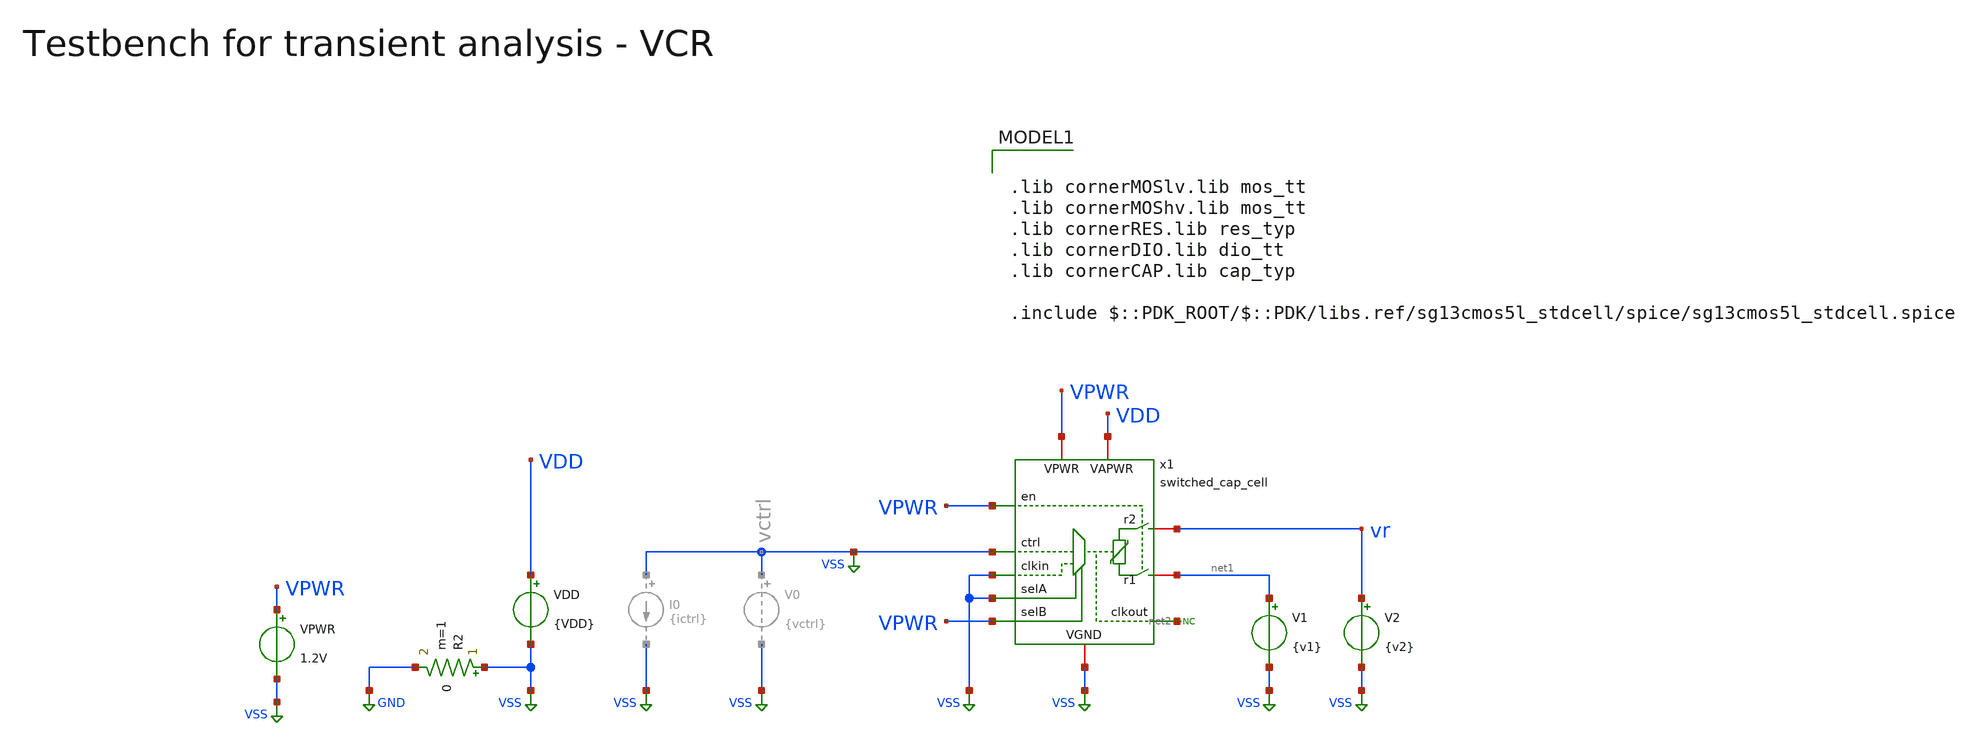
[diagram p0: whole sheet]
** sch_path: macros/heichips26_vcr/macros/switched_capacitor/testbenches/xschem/tb_switched_cap_tran.sch
**.subckt tb_switched_cap_tran
VDD VDD VSS {VDD}
R2 VSS GND 0 m=1
x1 VSS VDD VSS vr net1 VSS VSS VPWR VPWR VPWR net2 switched_cap_cell
V1 net1 VSS {v1}
V2 vr VSS {v2}
VPWR VPWR VSS 1.2V
* noconn #net2
**** begin user architecture code

.lib cornerMOSlv.lib mos_tt
.lib cornerMOShv.lib mos_tt
.lib cornerRES.lib res_typ
.lib cornerDIO.lib dio_tt
.lib cornerCAP.lib cap_typ

.include $::PDK_ROOT/$::PDK/libs.ref/sg13cmos5l_stdcell/spice/sg13cmos5l_stdcell.spice



.param temp=27
.param vctrl  = 0.1
.param f      = {2e6/vctrl}
*.param f = 75Meg

* Derived timing parameters
.param period = {1/f}
.param ton    = {period/2}
.csparam tstop  = {5*period}
.csparam tstep  = {period/100}
.param ictrl  = {f*3.3e-12}
.param tr     = {period/1000}
.param tf     = {period/1000}

.param VDD = 3.3
.csparam VDD=VDD
.param vdm = 3.3
.param vcm = {VDD/2}
.param v1  = {vcm - vdm/2}
.param v2  = {vcm + vdm/2}

.options savecurrents klu method=gear reltol=1e-6 abstol=1e-12 gmin=1e-15
.probe alli
.control

save all
set appendwrite

tran {$&tstep} {$&tstop}
remzerovec

save all
set appendwrite

write @schname\.raw
set appendwrite

*let r_var = vr/i(r1)
meas tran period_sim TRIG i(V1) VAL=1m RISE=1 TARG i(V1) VAL=1m RISE=2
meas tran n_periods TRIG i(V1) VAL=1m RISE=1 TARG i(V1) VAL=1m RISE=LAST
meas tran i_avg AVG i(V1) FROM=0 TO=n_periods
meas tran v_avg AVG vr FROM=0 TO=n_periods
*meas tran r_avg AVG r_var

let npts = length(time) - 1
let i_mavg = integ(i(V1))[1, npts] / time[1, npts]
let v_mavg = integ(vr)[1, npts] / time[1, npts]
let r_mavg = v_mavg/i_mavg
let r_avg = v_avg/i_avg
let f_sim = 1/period_sim
let plot_y_lim = 1.2*r_avg

print period_sim f_sim r_avg

* Plotting
plot vr v_avg v_mavg
plot i(V1) i_avg i_mavg
plot r_avg r_mavg ylimit 0 $&plot_y_lim
plot x1.clk

* Write Data
unset appendwrite
set wr_vecnames
set wr_singlescale
wrdata ../plot_simulations/data/@schname\.txt v(vr) v(VDD) i(V1)

*quit
.endc


**** end user architecture code
**.ends

* expanding   symbol:  switched_cap_cell.sym # of pins=11
** sym_path: macros/heichips26_vcr/macros/switched_capacitor/schematic/xschem/switched_cap_cell.sym
** sch_path: macros/heichips26_vcr/macros/switched_capacitor/schematic/xschem/switched_cap_cell.sch
.subckt switched_cap_cell ctrl VAPWR VGND r2 r1 clkin selA selB en VPWR clkout
*.iopin r1
*.iopin r2
*.iopin VAPWR
*.iopin VGND
*.ipin ctrl
*.ipin clkin
*.ipin selA
*.ipin selB
*.ipin en
*.opin clkout
*.iopin VPWR
x2 out1 r1 c_sw nout1 VAPWR VGND transmission_gate
x6 out2 r2 c_sw nout2 VAPWR VGND transmission_gate
x1 VAPWR net3 net9 VGND net15 net16 osc
x4 net5 VAPWR clk VGND net3 net13 net1 net2 net6 net7 net8 hv_mux4
x5 VAPWR net2 VGND net17 net1 net18 vco
x3 out1 nout1 VAPWR clk VGND out2 nout2 net4 net14 pulse_shaper_en
x7 net11 net10 net5 net6 VAPWR VGND net7 net8 hv_binary_decoder4
* noconn #net18
* noconn #net19
* noconn #net15
* noconn #net16
* noconn #net17
x8 net12 ctrl net9 net7 VAPWR VGND transmission_gate
x9 VAPWR net7 net12 VGND hv_inverter_40u
x10 VAPWR clkin net13 VGND lvl_shift_up
x11 VAPWR selA net10 VGND lvl_shift_up
x12 VAPWR selB net11 VGND lvl_shift_up
x13 VAPWR en net4 VGND lvl_shift_up
x14 VPWR clk clkout VGND hv_inverter_40u
x15 VAPWR net4 net14 VGND hv_inverter_40u
x16 net4 ctrl net1 net14 VAPWR VGND transmission_gate
.ends


* expanding   symbol:  transmission_gate.sym # of pins=6
** sym_path: macros/heichips26_vcr/macros/switched_capacitor/schematic/xschem/transmission_gate.sym
** sch_path: macros/heichips26_vcr/macros/switched_capacitor/schematic/xschem/transmission_gate.sch
.subckt transmission_gate vctrl vin vout nvctrl VDD VSS
*.iopin vin
*.iopin vout
*.ipin vctrl
*.ipin nvctrl
*.iopin VDD
*.iopin VSS
XM3 vout vctrl vin VSS sg13_hv_nmos w={tg_ngate_w*tg_ng} l={tg_ch_len} ng={tg_ng} m=1 mm_ok=1
XM4 vout nvctrl vin VDD sg13_hv_pmos w={tg_pgate_w*tg_ng} l={tg_ch_len} ng={tg_ng} m=1 mm_ok=1
**** begin user architecture code


.param tg_ch_len=0.45u
.param tg_ngate_w=2u
.param tg_pgate_w=5u
.param tg_ng=20


**** end user architecture code
.ends


* expanding   symbol:  osc.sym # of pins=6
** sym_path: macros/heichips26_vcr/macros/switched_capacitor/schematic/xschem/osc.sym
** sch_path: macros/heichips26_vcr/macros/switched_capacitor/schematic/xschem/osc.sch
.subckt osc VDD out1 ictrl VSS start out2
*.iopin VSS
*.iopin VDD
*.iopin out2
*.iopin out1
*.iopin start
*.iopin ictrl
XM3 out1 ictrl VDD VDD sg13_hv_pmos w=10.0u l=2.0u ng=1 m=1 mm_ok=1
XM2 net1 ictrl VDD VDD sg13_hv_pmos w=1u l=2.0u ng=1 m=1 mm_ok=1
XM4 start ictrl VDD VDD sg13_hv_pmos w=1.0u l=2.0u ng=1 m=1 mm_ok=1
XM5 out2 ictrl VDD VDD sg13_hv_pmos w=10.0u l=2.0u ng=1 m=1 mm_ok=1
XM6 ictrl ictrl VDD VDD sg13_hv_pmos w=10.0u l=2.0u ng=1 m=1 mm_ok=1
XC1 net1 out1 cap_cmomi w=10e-6 l=10e-6 mmin=1 mmax=4 feed=double subblock=0 m=1 mm_ok=1
XC2 out2 start cap_cmomi w=10e-6 l=10e-6 mmin=1 mmax=4 feed=double subblock=0 m=1 mm_ok=1
XM8 out1 start VSS VSS sg13_hv_nmos w=3u l=0.45u ng=1 m=1 mm_ok=1
XM1 start start VSS VSS sg13_hv_nmos w=1u l=2u ng=1 m=1 mm_ok=1
XM12 out2 net1 VSS VSS sg13_hv_nmos w=3u l=0.45u ng=1 m=1 mm_ok=1
XM11 net1 net1 VSS VSS sg13_hv_nmos w=1u l=2u ng=1 m=1 mm_ok=1
**** begin user architecture code


.ic v(out1)=0 v(out2)=3.3


**** end user architecture code
.ends


* expanding   symbol:  hv_mux4.sym # of pins=11
** sym_path: macros/heichips26_vcr/macros/switched_capacitor/schematic/xschem/hv_mux4.sym
** sch_path: macros/heichips26_vcr/macros/switched_capacitor/schematic/xschem/hv_mux4.sch
.subckt hv_mux4 nsel1 VDD out VSS in3 in1 in4 in2 nsel2 nsel3 nsel4
*.ipin in1
*.iopin VDD
*.iopin VSS
*.opin out
*.ipin in2
*.ipin in3
*.ipin in4
*.ipin nsel1
*.ipin nsel3
*.ipin nsel2
*.ipin nsel4
x1 VDD net2 out net1 VSS net3 net4 hv_nor4
x2 VDD nsel1 net2 in1 VSS hv_nor
x4 VDD nsel2 net1 in2 VSS hv_nor
x5 VDD nsel3 net3 in3 VSS hv_nor
x6 VDD nsel4 net4 in4 VSS hv_nor
.ends


* expanding   symbol:  vco.sym # of pins=6
** sym_path: macros/heichips26_vcr/macros/switched_capacitor/schematic/xschem/vco.sym
** sch_path: macros/heichips26_vcr/macros/switched_capacitor/schematic/xschem/vco.sch
.subckt vco VDD out VSS nout vctrl vc
*.iopin VSS
*.iopin VDD
*.iopin nout
*.iopin out
*.iopin vctrl
*.iopin vc
**** begin user architecture code


.ic v(vc)=1.65


**** end user architecture code
XC1 vc VSS cap_cmomi w=30e-6 l=30e-6 mmin=1 mmax=4 feed=double subblock=0 m=1 mm_ok=1
XM4 vc out 5uA- VSS sg13_hv_nmos w=0.3u l=0.45u ng=1 m=1 mm_ok=1
x1 VDD s out nout r VSS hv_rs-ff
**** begin user architecture code


.param cm_n_w = 6u
.param cm_n_l = 5u
.param cm_p_w = 10u
.param cm_p_l = 2u

.param inv_ng = 1
.param inv_n_w = 2u
.param inv_n_l = 0.45u
.param inv_p_w = 6.5u
.param inv_p_l = 0.4u


**** end user architecture code
XM6 vc out 5uA+ VDD sg13_hv_pmos w=0.3u l=0.4u ng=1 m=1 mm_ok=1
x5 net2 vc vthl VDD 40uA- VSS comp_pmos
x7 net1 vthh vc VDD 40uA+ VSS comp_nmos
x2 10uA- vthl VDD vctrl VSS vthh voltage_mirror_pmos
x3 VDD net1 s VSS hv_inverter_6u5
x6 VDD net2 r VSS hv_inverter_6u5
x8 40uA+ 5uA+ VDD VSS 5uA- 10uA- 40uA- bias_current_generator
.ends


* expanding   symbol:  pulse_shaper_en.sym # of pins=9
** sym_path: macros/heichips26_vcr/macros/switched_capacitor/schematic/xschem/pulse_shaper_en.sym
** sch_path: macros/heichips26_vcr/macros/switched_capacitor/schematic/xschem/pulse_shaper_en.sch
.subckt pulse_shaper_en out1 nout1 VDD in VSS out2 nout2 en dis
*.opin out1
*.opin nout1
*.opin out2
*.opin nout2
*.ipin in
*.iopin VSS
*.iopin VDD
*.ipin en
*.ipin dis
x7 VDD net1 net3 VSS low_th_inverter
x8 VDD net1 net2 VSS high_th_inverter
x10 VDD out1 nout1 VSS hv_inverter_40u
x11 VDD nout2 out2 VSS hv_inverter_40u
**** begin user architecture code


.include ../../../netlist/pex/hv_inverter_0u3_magic_pex_3.spice
.param w   = 0.3u
.param ng  = 1
.param n_ng = ng
.param n_w = {w*n_ng}
.param n_l = 0.45u
.param p_ng = ng
.param p_w = {1*w*p_ng}
.param p_l = 0.4u


**** end user architecture code
x1 VDD in net1 VSS hv_inverter_0u3
x5 VDD net2 out1 dis VSS hv_nor
x4 VDD net3 nout2 en VSS hv_nand
.ends


* expanding   symbol:  hv_binary_decoder4.sym # of pins=8
** sym_path: macros/heichips26_vcr/macros/switched_capacitor/schematic/xschem/hv_binary_decoder4.sym
** sch_path: macros/heichips26_vcr/macros/switched_capacitor/schematic/xschem/hv_binary_decoder4.sch
.subckt hv_binary_decoder4 msb lsb nout1 nout2 VDD VSS nout3 nout4
*.iopin VDD
*.iopin VSS
*.ipin msb
*.ipin lsb
*.opin nout1
*.opin nout2
*.opin nout3
*.opin nout4
x3 VDD msb net1 VSS hv_inverter_40u
x7 VDD msb nout4 lsb VSS hv_nand
x9 VDD net1 nout2 lsb VSS hv_nand
x10 VDD lsb net2 VSS hv_inverter_40u
x11 VDD msb nout3 net2 VSS hv_nand
x8 VDD net1 nout1 net2 VSS hv_nand
.ends


* expanding   symbol:  hv_inverter_40u.sym # of pins=4
** sym_path: macros/heichips26_vcr/macros/switched_capacitor/schematic/xschem/hv_inverter_40u.sym
** sch_path: macros/heichips26_vcr/macros/switched_capacitor/schematic/xschem/hv_inverter_40u.sch
.subckt hv_inverter_40u VDD in out VSS
*.ipin in
*.iopin VDD
*.iopin VSS
*.opin out
XM2 out in VSS VSS sg13_hv_nmos w={n_w} l={n_l} ng={ng} m=1 mm_ok=1
XM3 out in VDD VDD sg13_hv_pmos w={p_w} l={p_l} ng={ng} m=1 mm_ok=1
**** begin user architecture code


.param w   = 10u
.param ng  = 4
.param n_ng = ng
.param n_w = {3u*n_ng}
.param n_l = 0.45u
.param p_ng = ng
.param p_w = {10u*p_ng}
.param p_l = 0.4u


**** end user architecture code
.ends


* expanding   symbol:  lvl_shift_up.sym # of pins=4
** sym_path: macros/heichips26_vcr/macros/switched_capacitor/schematic/xschem/lvl_shift_up.sym
** sch_path: macros/heichips26_vcr/macros/switched_capacitor/schematic/xschem/lvl_shift_up.sch
.subckt lvl_shift_up VDD in out VSS
*.ipin in
*.iopin VDD
*.iopin VSS
*.opin out
XM1 net1 in VSS VSS sg13_hv_nmos w={n_ng*n_w} l={n_l} ng={n_ng} m=1 mm_ok=1
XM2 net1 in VDD VDD sg13_hv_pmos w={p_ng*p_w} l={p_l} ng={n_ng} m=1 mm_ok=1
**** begin user architecture code


.param n_ng = 2
.param n_w = 10u
.param n_l = 0.45u
.param p_ng = 2
.param p_w = 1u
.param p_l = 0.45u


**** end user architecture code
x4 VDD net1 out VSS hv_inverter_6u5
.ends


* expanding   symbol:  hv_nor4.sym # of pins=7
** sym_path: macros/heichips26_vcr/macros/switched_capacitor/schematic/xschem/hv_nor4.sym
** sch_path: macros/heichips26_vcr/macros/switched_capacitor/schematic/xschem/hv_nor4.sch
.subckt hv_nor4 VDD in1 out in2 VSS in3 in4
*.ipin in1
*.iopin VDD
*.iopin VSS
*.opin out
*.ipin in2
*.ipin in3
*.ipin in4
**** begin user architecture code


.param w   = 10u
.param ng  = 4
.param n_ng = ng
.param n_w = {3u*n_ng}
.param n_l = 0.45u
.param p_ng = ng
.param p_w = {10u*p_ng}
.param p_l = 0.4u


**** end user architecture code
XM2 out in3 VSS VSS sg13_hv_nmos w={n_w} l={n_l} ng={ng} m=1 mm_ok=1
XM3 net3 in4 VDD VDD sg13_hv_pmos w={p_w} l={p_l} ng={ng} m=1 mm_ok=1
XM1 out in4 VSS VSS sg13_hv_nmos w={n_w} l={n_l} ng={ng} m=1 mm_ok=1
XM4 out in1 net1 VDD sg13_hv_pmos w={p_w} l={p_l} ng={ng} m=1 mm_ok=1
XM5 out in2 VSS VSS sg13_hv_nmos w={n_w} l={n_l} ng={ng} m=1 mm_ok=1
XM6 out in1 VSS VSS sg13_hv_nmos w={n_w} l={n_l} ng={ng} m=1 mm_ok=1
XM7 net1 in2 net2 VDD sg13_hv_pmos w={p_w} l={p_l} ng={ng} m=1 mm_ok=1
XM8 net2 in3 net3 VDD sg13_hv_pmos w={p_w} l={p_l} ng={ng} m=1 mm_ok=1
.ends


* expanding   symbol:  hv_nor.sym # of pins=5
** sym_path: macros/heichips26_vcr/macros/switched_capacitor/schematic/xschem/hv_nor.sym
** sch_path: macros/heichips26_vcr/macros/switched_capacitor/schematic/xschem/hv_nor.sch
.subckt hv_nor VDD in1 out in2 VSS
*.ipin in1
*.iopin VDD
*.iopin VSS
*.opin out
*.ipin in2
**** begin user architecture code


.param w   = 10u
.param ng  = 4
.param n_ng = ng
.param n_w = {3u*n_ng}
.param n_l = 0.45u
.param p_ng = ng
.param p_w = {10u*p_ng}
.param p_l = 0.4u


**** end user architecture code
XM2 out in1 VSS VSS sg13_hv_nmos w={n_w} l={n_l} ng={ng} m=1 mm_ok=1
XM3 net1 in2 VDD VDD sg13_hv_pmos w={p_w} l={p_l} ng={ng} m=1 mm_ok=1
XM1 out in2 VSS VSS sg13_hv_nmos w={n_w} l={n_l} ng={ng} m=1 mm_ok=1
XM4 out in1 net1 VDD sg13_hv_pmos w={p_w} l={p_l} ng={ng} m=1 mm_ok=1
.ends


* expanding   symbol:  hv_rs-ff.sym # of pins=6
** sym_path: macros/heichips26_vcr/macros/switched_capacitor/schematic/xschem/hv_rs-ff.sym
** sch_path: macros/heichips26_vcr/macros/switched_capacitor/schematic/xschem/hv_rs-ff.sch
.subckt hv_rs-ff VDD nS Q nQ nR VSS
*.ipin nS
*.iopin VDD
*.iopin VSS
*.opin Q
*.ipin nR
*.opin nQ
x4 VDD nS Q nQ VSS hv_nand
x5 VDD Q nQ nR VSS hv_nand
.ends


* expanding   symbol:  comp_pmos.sym # of pins=6
** sym_path: macros/heichips26_vcr/macros/switched_capacitor/schematic/xschem/comp_pmos.sym
** sch_path: macros/heichips26_vcr/macros/switched_capacitor/schematic/xschem/comp_pmos.sch
.subckt comp_pmos out - + VDD Ibias VSS
*.iopin VDD
*.iopin VSS
*.ipin Ibias
*.opin out
*.ipin +
*.ipin -
**** begin user architecture code


.param n_w = 1.2u
.param n_l = 1.5u
.param p_w = 2u
.param p_l = 0.4u
.param bcm = 1


**** end user architecture code
XM9 net1 Ibias VDD VDD sg13_hv_pmos w=bcm*p_w l=p_l ng=1 m=1 mm_ok=1
XM10 out Ibias VDD VDD sg13_hv_pmos w=bcm*p_w l=p_l ng=1 m=1 mm_ok=1
XM11 Ibias Ibias VDD VDD sg13_hv_pmos w=p_w l=p_l ng=1 m=1 mm_ok=1
XM12 net3 + net1 VDD sg13_hv_pmos w=p_w l=p_l ng=1 m=1 mm_ok=1
XM13 net2 - net1 VDD sg13_hv_pmos w=p_w l=p_l ng=1 m=1 mm_ok=1
XM14 net3 net2 VSS VSS sg13_hv_nmos w=n_w l=n_l ng=1 m=1 mm_ok=1
XM15 net2 net2 VSS VSS sg13_hv_nmos w=n_w l=n_l ng=1 m=1 mm_ok=1
XM16 out net3 VSS VSS sg13_hv_nmos w=n_w l=n_l ng=1 m=1 mm_ok=1
.ends


* expanding   symbol:  comp_nmos.sym # of pins=6
** sym_path: macros/heichips26_vcr/macros/switched_capacitor/schematic/xschem/comp_nmos.sym
** sch_path: macros/heichips26_vcr/macros/switched_capacitor/schematic/xschem/comp_nmos.sch
.subckt comp_nmos out - + VDD Ibias VSS
*.iopin VDD
*.iopin VSS
*.ipin -
*.ipin +
*.ipin Ibias
*.opin out
XM8 net2 + net3 VSS sg13_hv_nmos w=n_w l=n_l ng=1 m=1 mm_ok=1
XM6 net1 net1 VDD VDD sg13_hv_pmos w=p_w l=p_l ng=1 m=1 mm_ok=1
XM1 net2 net1 VDD VDD sg13_hv_pmos w=p_w l=p_l ng=1 m=1 mm_ok=1
XM3 net1 - net3 VSS sg13_hv_nmos w=n_w l=n_l ng=1 m=1 mm_ok=1
**** begin user architecture code


.param n_w = 1.2u
.param n_l = 1.5u
.param p_w = 2u
.param p_l = 0.4u


**** end user architecture code
XM2 out net2 VDD VDD sg13_hv_pmos w=p_w l=p_l ng=1 m=1 mm_ok=1
XM4 net3 Ibias VSS VSS sg13_hv_nmos w=2*n_w l=n_l ng=1 m=1 mm_ok=1
XM5 out Ibias VSS VSS sg13_hv_nmos w=2*n_w l=n_l ng=1 m=1 mm_ok=1
XM7 Ibias Ibias VSS VSS sg13_hv_nmos w=n_w l=n_l ng=1 m=1 mm_ok=1
.ends


* expanding   symbol:  voltage_mirror_pmos.sym # of pins=6
** sym_path: macros/heichips26_vcr/macros/switched_capacitor/schematic/xschem/voltage_mirror_pmos.sym
** sch_path: macros/heichips26_vcr/macros/switched_capacitor/schematic/xschem/voltage_mirror_pmos.sch
.subckt voltage_mirror_pmos Ibias nout VDD in VSS out
*.iopin VDD
*.iopin VSS
*.ipin in
*.opin out
*.opin nout
*.ipin Ibias
**** begin user architecture code


.param n_w = 6u
.param n_l = 5u
.param p_w = 10u
.param p_l = 2u


**** end user architecture code
XR1 in Ibias VSS rhigh w=0.5e-6 l=34e-6 m=1 b=0 mm_ok=1
XM4 net1 Ibias VDD VDD sg13_hv_pmos w=p_w l=p_l ng=1 m=1 mm_ok=1
XM5 out net1 VSS VSS sg13_hv_nmos w=n_w l=n_l ng=1 m=1 mm_ok=1
XR2 VSS nout VSS rhigh w=0.5e-6 l=34e-6 m=1 b=0 mm_ok=1
XR3 out VDD VSS rhigh w=0.5e-6 l=34e-6 m=1 b=0 mm_ok=1
XM2 net1 net1 VSS VSS sg13_hv_nmos w=n_w l=n_l ng=1 m=1 mm_ok=1
XM3 nout Ibias VDD VDD sg13_hv_pmos w=p_w l=p_l ng=1 m=1 mm_ok=1
XM6 Ibias Ibias VDD VDD sg13_hv_pmos w=1.9*p_w l=p_l ng=1 m=1 mm_ok=1
.ends


* expanding   symbol:  hv_inverter_6u5.sym # of pins=4
** sym_path: macros/heichips26_vcr/macros/switched_capacitor/schematic/xschem/hv_inverter_6u5.sym
** sch_path: macros/heichips26_vcr/macros/switched_capacitor/schematic/xschem/hv_inverter_6u5.sch
.subckt hv_inverter_6u5 VDD in out VSS
*.ipin in
*.iopin VDD
*.iopin VSS
*.opin out
XM2 out in VSS VSS sg13_hv_nmos w={n_w} l={n_l} ng={ng} m=1 mm_ok=1
XM3 out in VDD VDD sg13_hv_pmos w={p_w} l={p_l} ng={ng} m=1 mm_ok=1
**** begin user architecture code


.param ng  = 1
.param n_ng = ng
.param n_w = {2u*n_ng}
.param n_l = 0.45u
.param p_ng = ng
.param p_w = {6.5u*p_ng}
.param p_l = 0.4u


**** end user architecture code
.ends


* expanding   symbol:  bias_current_generator.sym # of pins=7
** sym_path: macros/heichips26_vcr/macros/switched_capacitor/schematic/xschem/bias_current_generator.sym
** sch_path: macros/heichips26_vcr/macros/switched_capacitor/schematic/xschem/bias_current_generator.sch
.subckt bias_current_generator 40uA+ 5uA+ VDD VSS 5uA- 10uA- 40uA-
*.opin 40uA+
*.iopin VSS
*.iopin VDD
*.opin 40uA-
*.opin 10uA-
*.opin 5uA+
*.opin 5uA-
x4 VDD net1 VSS current_reference_40uA
XM11 net1 net1 VDD VDD sg13_hv_pmos w=cm_p_w l=cm_p_l ng=1 m=1 mm_ok=1
XM12 40uA+ net1 VDD VDD sg13_hv_pmos w=cm_p_w l=cm_p_l ng=1 m=1 mm_ok=1
XM13 net2 net1 VDD VDD sg13_hv_pmos w=cm_p_w l=cm_p_l ng=1 m=1 mm_ok=1
XM14 net2 net2 VSS VSS sg13_hv_nmos w=cm_n_w l=cm_n_l ng=1 m=1 mm_ok=1
XM15 40uA- net2 VSS VSS sg13_hv_nmos w=cm_n_w l=cm_n_l ng=1 m=1 mm_ok=1
XM1 net3 net1 VDD VDD sg13_hv_pmos w=cm_p_w l=cm_p_l ng=1 m=1 mm_ok=1
XM2 net3 net3 VSS VSS sg13_hv_nmos w=4*cm_n_w l=cm_n_l ng=4 m=1 mm_ok=1
XM3 10uA- net3 VSS VSS sg13_hv_nmos w=cm_n_w l=cm_n_l ng=1 m=1 mm_ok=1
XM5 net4 net3 VSS VSS sg13_hv_nmos w=cm_n_w l=cm_n_l ng=1 m=1 mm_ok=1
XM25 net4 net4 VDD VDD sg13_hv_pmos w=2*cm_p_w l=cm_p_l ng=2 m=1 mm_ok=1
XM26 net5 net4 VDD VDD sg13_hv_pmos w=cm_p_w l=cm_p_l ng=1 m=1 mm_ok=1
XM27 5uA+ net4 VDD VDD sg13_hv_pmos w=cm_p_w l=cm_p_l ng=1 m=1 mm_ok=1
XM28 net5 net5 VSS VSS sg13_hv_nmos w=cm_n_w l=cm_n_l ng=2 m=1 mm_ok=1
XM29 5uA- net5 VSS VSS sg13_hv_nmos w=cm_n_w l=cm_n_l ng=1 m=1 mm_ok=1
**** begin user architecture code


.param cm_n_w = 6u
.param cm_n_l = 5u
.param cm_p_w = 10u
.param cm_p_l = 2u


**** end user architecture code
.ends


* expanding   symbol:  low_th_inverter.sym # of pins=4
** sym_path: macros/heichips26_vcr/macros/switched_capacitor/schematic/xschem/low_th_inverter.sym
** sch_path: macros/heichips26_vcr/macros/switched_capacitor/schematic/xschem/low_th_inverter.sch
.subckt low_th_inverter VDD vin vout VSS
*.ipin vin
*.iopin VDD
*.iopin VSS
*.opin vout
XM1 vout vin VSS VSS sg13_hv_nmos w={n_ng*n_w} l={n_l} ng={n_ng} m=1 mm_ok=1
XM2 vout vin VDD VDD sg13_hv_pmos w={p_ng*p_w} l={p_l} ng={n_ng} m=1 mm_ok=1
**** begin user architecture code


.param n_ng = 2
.param n_w = 1u
.param n_l = 0.45u
.param p_ng = 2
.param p_w = 1u
.param p_l = 0.4u


**** end user architecture code
.ends


* expanding   symbol:  high_th_inverter.sym # of pins=4
** sym_path: macros/heichips26_vcr/macros/switched_capacitor/schematic/xschem/high_th_inverter.sym
** sch_path: macros/heichips26_vcr/macros/switched_capacitor/schematic/xschem/high_th_inverter.sch
.subckt high_th_inverter VDD vin vout VSS
*.ipin vin
*.iopin VDD
*.iopin VSS
*.opin vout
XMdummy1 VSS VSS VSS VSS sg13_hv_nmos w=0.6u l=1.0u ng=2 m=1 mm_ok=1
XMdummy2 VDD VDD VDD VDD sg13_hv_pmos w=12.0u l=1.0u ng=2 m=1 mm_ok=1
XM1 vout vin VSS VSS sg13_hv_nmos w=6.0u l=1.0u ng=20 m=1 mm_ok=1
XM2 vout vin VDD VDD sg13_hv_pmos w=120.0u l=1.0u ng=20 m=1 mm_ok=1
.ends


* expanding   symbol:  hv_inverter_0u3.sym # of pins=4
** sym_path: macros/heichips26_vcr/macros/switched_capacitor/schematic/xschem/hv_inverter_0u3.sym
** sch_path: macros/heichips26_vcr/macros/switched_capacitor/schematic/xschem/hv_inverter_0u3.sch
.subckt hv_inverter_0u3 VDD in out VSS
*.ipin in
*.iopin VDD
*.iopin VSS
*.opin out
XM2 out in VSS VSS sg13_hv_nmos w={n_w} l={n_l} ng={ng} m=1 mm_ok=1
XM3 out in VDD VDD sg13_hv_pmos w={p_w} l={p_l} ng={ng} m=1 mm_ok=1
**** begin user architecture code


.param w   = 0.3u
.param ng  = 1
.param n_ng = ng
.param n_w = {w*n_ng}
.param n_l = 0.45u
.param p_ng = ng
.param p_w = {1*w*p_ng}
.param p_l = 0.4u


**** end user architecture code
.ends


* expanding   symbol:  hv_nand.sym # of pins=5
** sym_path: macros/heichips26_vcr/macros/switched_capacitor/schematic/xschem/hv_nand.sym
** sch_path: macros/heichips26_vcr/macros/switched_capacitor/schematic/xschem/hv_nand.sch
.subckt hv_nand VDD in1 out in2 VSS
*.ipin in1
*.iopin VDD
*.iopin VSS
*.opin out
*.ipin in2
**** begin user architecture code


.param w   = 10u
.param ng  = 4
.param n_ng = ng
.param n_w = {3u*n_ng}
.param n_l = 0.45u
.param p_ng = ng
.param p_w = {10u*p_ng}
.param p_l = 0.4u


**** end user architecture code
XM2 out in1 net1 VSS sg13_hv_nmos w={n_w} l={n_l} ng={ng} m=1 mm_ok=1
XM3 out in2 VDD VDD sg13_hv_pmos w={p_w} l={p_l} ng={ng} m=1 mm_ok=1
XM1 net1 in2 VSS VSS sg13_hv_nmos w={n_w} l={n_l} ng={ng} m=1 mm_ok=1
XM4 out in1 VDD VDD sg13_hv_pmos w={p_w} l={p_l} ng={ng} m=1 mm_ok=1
.ends


* expanding   symbol:  current_reference_40uA.sym # of pins=3
** sym_path: macros/heichips26_vcr/macros/switched_capacitor/schematic/xschem/current_reference_40uA.sym
** sch_path: macros/heichips26_vcr/macros/switched_capacitor/schematic/xschem/current_reference_40uA.sch
.subckt current_reference_40uA VDD iout VSS
*.iopin VSS
*.iopin VDD
*.iopin iout
XM8 net2 net2 VSS VSS sg13_hv_nmos w=n_w l=n_l ng=1 m=1 mm_ok=1
XM6 net2 net1 VDD VDD sg13_hv_pmos w=p_w l=p_l ng=1 m=1 mm_ok=1
XM1 net1 net1 VDD VDD sg13_hv_pmos w=p_w l=p_l ng=1 m=1 mm_ok=1
XM3 net1 net2 net3 VSS sg13_hv_nmos w=n_w l=n_l ng=1 m=1 mm_ok=1
XR2 net4 VSS VSS rppd w=2e-6 l=21.9e-6 m=1 b=0 mm_ok=1
XM2 net1 net2 net3 VSS sg13_hv_nmos w=n_w l=n_l ng=1 m=1 mm_ok=1
XM4 net1 net2 net3 VSS sg13_hv_nmos w=n_w l=n_l ng=1 m=1 mm_ok=1
XM5 net1 net2 net3 VSS sg13_hv_nmos w=n_w l=n_l ng=1 m=1 mm_ok=1
XM7 iout net2 VSS VSS sg13_hv_nmos w=n_w l=n_l ng=1 m=1 mm_ok=1
XR3 net3 net4 VSS rsil w=0.5e-6 l=365e-6 m=1 mm_ok=1
**** begin user architecture code


.param n_w = 6u
.param n_l = 5u
.param p_w = 10u
.param p_l = 2u


**** end user architecture code
.ends

.GLOBAL VSS
.GLOBAL GND
.end
